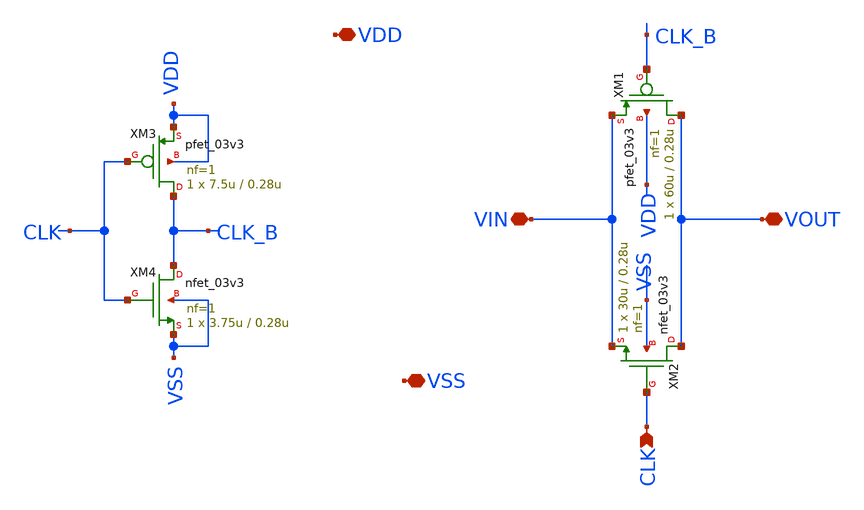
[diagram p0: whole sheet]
** sch_path: SCOP_INPUT_AND_MUX_PAKISTAN_03/Xschem/Logic_Gates/Transmission_Gate.sch
**.subckt Transmission_Gate VIN VOUT CLK VDD VSS
*.iopin VIN
*.iopin VOUT
*.ipin CLK
*.iopin VDD
*.iopin VSS
XM1 VOUT CLK_B VIN VDD pfet_03v3 L=0.28u W=60u nf=1 ad='int((nf+1)/2) * W/nf * 0.18u' as='int((nf+2)/2) * W/nf * 0.18u'
+ pd='2*int((nf+1)/2) * (W/nf + 0.18u)' ps='2*int((nf+2)/2) * (W/nf + 0.18u)' nrd='0.18u / W' nrs='0.18u / W'
+ sa=0 sb=0 sd=0 m=1
XM2 VOUT CLK VIN VSS nfet_03v3 L=0.28u W=30u nf=1 ad='int((nf+1)/2) * W/nf * 0.18u' as='int((nf+2)/2) * W/nf * 0.18u'
+ pd='2*int((nf+1)/2) * (W/nf + 0.18u)' ps='2*int((nf+2)/2) * (W/nf + 0.18u)' nrd='0.18u / W' nrs='0.18u / W'
+ sa=0 sb=0 sd=0 m=1
XM3 CLK_B CLK VDD VDD pfet_03v3 L=0.28u W=7.5u nf=1 ad='int((nf+1)/2) * W/nf * 0.18u' as='int((nf+2)/2) * W/nf * 0.18u'
+ pd='2*int((nf+1)/2) * (W/nf + 0.18u)' ps='2*int((nf+2)/2) * (W/nf + 0.18u)' nrd='0.18u / W' nrs='0.18u / W'
+ sa=0 sb=0 sd=0 m=1
XM4 CLK_B CLK VSS VSS nfet_03v3 L=0.28u W=3.75u nf=1 ad='int((nf+1)/2) * W/nf * 0.18u' as='int((nf+2)/2) * W/nf * 0.18u'
+ pd='2*int((nf+1)/2) * (W/nf + 0.18u)' ps='2*int((nf+2)/2) * (W/nf + 0.18u)' nrd='0.18u / W' nrs='0.18u / W'
+ sa=0 sb=0 sd=0 m=1
**.ends
.end
